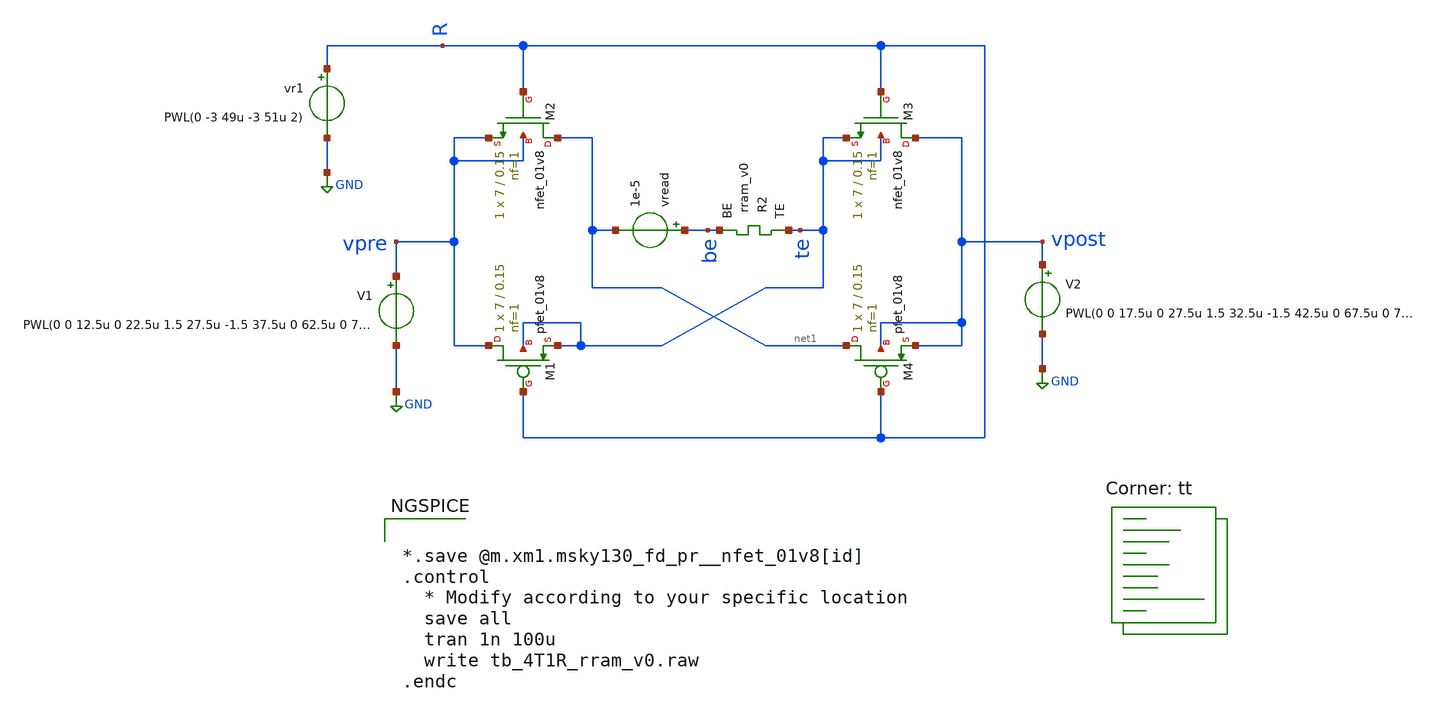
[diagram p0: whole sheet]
** sch_path: Synapse/tb_4T1R_rram_v0.sch
**.subckt tb_4T1R_rram_v0
XR2 te be rram_v0
XM2 net1 R vpre vpre sky130_fd_pr__nfet_01v8 L=0.15 W=7 nf=1 ad='int((nf+1)/2) * W/nf * 0.29' as='int((nf+2)/2) * W/nf * 0.29'
+ pd='2*int((nf+1)/2) * (W/nf + 0.29)' ps='2*int((nf+2)/2) * (W/nf + 0.29)' nrd='0.29 / W' nrs='0.29 / W'
+ sa=0 sb=0 sd=0 mult=1 m=1
XM3 vpost R te te sky130_fd_pr__nfet_01v8 L=0.15 W=7 nf=1 ad='int((nf+1)/2) * W/nf * 0.29' as='int((nf+2)/2) * W/nf * 0.29'
+ pd='2*int((nf+1)/2) * (W/nf + 0.29)' ps='2*int((nf+2)/2) * (W/nf + 0.29)' nrd='0.29 / W' nrs='0.29 / W'
+ sa=0 sb=0 sd=0 mult=1 m=1
V1 vpre GND PWL(0 0 12.5u 0 22.5u 1.5 27.5u -1.5 37.5u 0 62.5u 0 72.5u 1.5 77.5u -1.5 87.5u 0)
V2 vpost GND PWL(0 0 17.5u 0 27.5u 1.5 32.5u -1.5 42.5u 0 67.5u 0 77.5u 1.5 82.5u -1.5 92.5u 0)
vread be net1 1e-5
vr1 R GND PWL(0 -3 49u -3 51u 2)
XM1 vpre R te te sky130_fd_pr__pfet_01v8 L=0.15 W=7 nf=1 ad='int((nf+1)/2) * W/nf * 0.29' as='int((nf+2)/2) * W/nf * 0.29'
+ pd='2*int((nf+1)/2) * (W/nf + 0.29)' ps='2*int((nf+2)/2) * (W/nf + 0.29)' nrd='0.29 / W' nrs='0.29 / W'
+ sa=0 sb=0 sd=0 mult=1 m=1
XM4 net1 R vpost vpost sky130_fd_pr__pfet_01v8 L=0.15 W=7 nf=1 ad='int((nf+1)/2) * W/nf * 0.29' as='int((nf+2)/2) * W/nf * 0.29'
+ pd='2*int((nf+1)/2) * (W/nf + 0.29)' ps='2*int((nf+2)/2) * (W/nf + 0.29)' nrd='0.29 / W' nrs='0.29 / W'
+ sa=0 sb=0 sd=0 mult=1 m=1
**** begin user architecture code


*.save @m.xm1.msky130_fd_pr__nfet_01v8[id]
.control
  * Modify according to your specific location
  save all
  tran 1n 100u
  write tb_4T1R_rram_v0.raw
.endc



.lib $::SKYWATER_MODELS/sky130.lib.spice tt

** opencircuitdesign pdks install
.inc $::SKYWATER_MODELS/rram_v0.spice

**** end user architecture code
**.ends
.GLOBAL GND
.end
